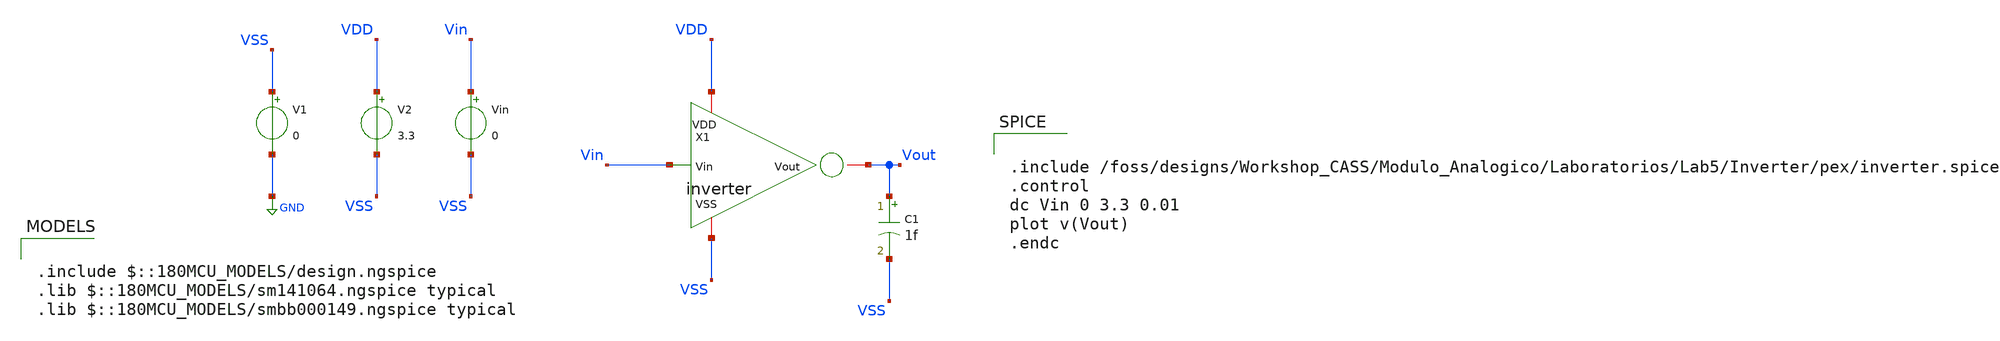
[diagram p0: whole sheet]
** sch_path: Modulo_Analogico/Laboratorios/Lab5/Inverter/pex/inverter_tb.sch
**.subckt inverter_tb
C1 Vout VSS 1f m=1
V1 VSS GND 0
V2 VDD VSS 3.3
Vin Vin VSS 0
X1 Vin VDD VSS Vout inverter
**** begin user architecture code

.include $::180MCU_MODELS/design.ngspice
.lib $::180MCU_MODELS/sm141064.ngspice typical
.lib $::180MCU_MODELS/smbb000149.ngspice typical



.include /foss/designs/Workshop_CASS/Modulo_Analogico/Laboratorios/Lab5/Inverter/pex/inverter.spice
.control
dc Vin 0 3.3 0.01
plot v(Vout)
.endc


**** end user architecture code
**.ends
.GLOBAL GND
.end
